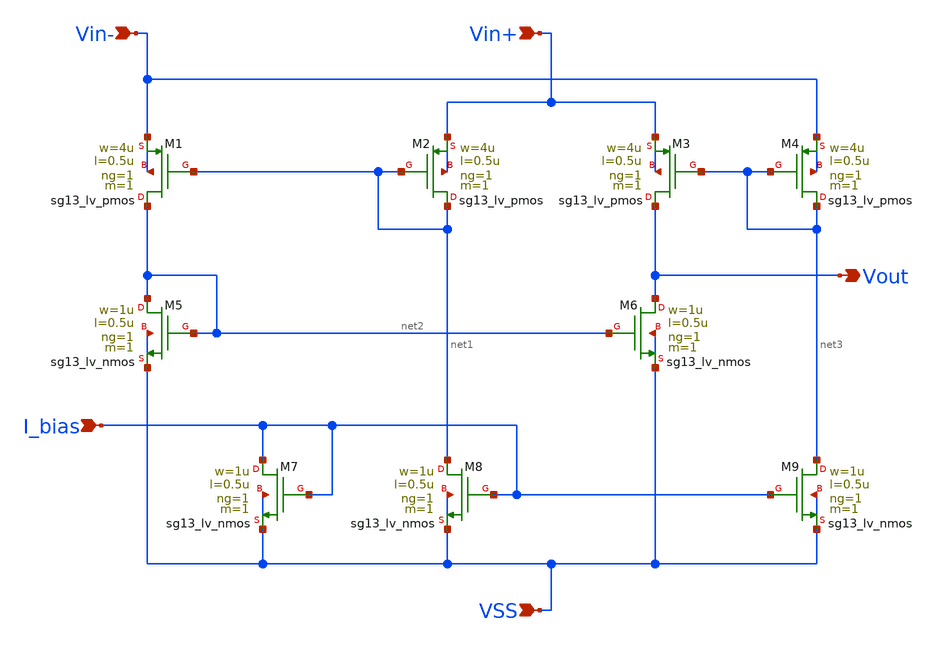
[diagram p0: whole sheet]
** sch_path: SSDOR_1.2V_v2/components/pmos_comp_old/pmos_comp.sch
**.subckt pmos_comp I_bias Vin- Vin+ VSS Vout
*.ipin I_bias
*.ipin Vin-
*.ipin Vin+
*.ipin VSS
*.opin Vout
XM1 net2 net1 Vin- Vin- sg13_lv_pmos w=4u l=0.5u ng=1 m=1 mm_ok=1
XM2 net1 net1 Vin+ Vin+ sg13_lv_pmos w=4u l=0.5u ng=1 m=1 mm_ok=1
XM3 Vout net3 Vin+ Vin+ sg13_lv_pmos w=4u l=0.5u ng=1 m=1 mm_ok=1
XM4 net3 net3 Vin- Vin- sg13_lv_pmos w=4u l=0.5u ng=1 m=1 mm_ok=1
XM5 net2 net2 VSS VSS sg13_lv_nmos w=1u l=0.5u ng=1 m=1 mm_ok=1
XM6 Vout net2 VSS VSS sg13_lv_nmos w=1u l=0.5u ng=1 m=1 mm_ok=1
XM7 I_bias I_bias VSS VSS sg13_lv_nmos w=1u l=0.5u ng=1 m=1 mm_ok=1
XM8 net1 I_bias VSS VSS sg13_lv_nmos w=1u l=0.5u ng=1 m=1 mm_ok=1
XM9 net3 I_bias VSS VSS sg13_lv_nmos w=1u l=0.5u ng=1 m=1 mm_ok=1
**.ends
.end
